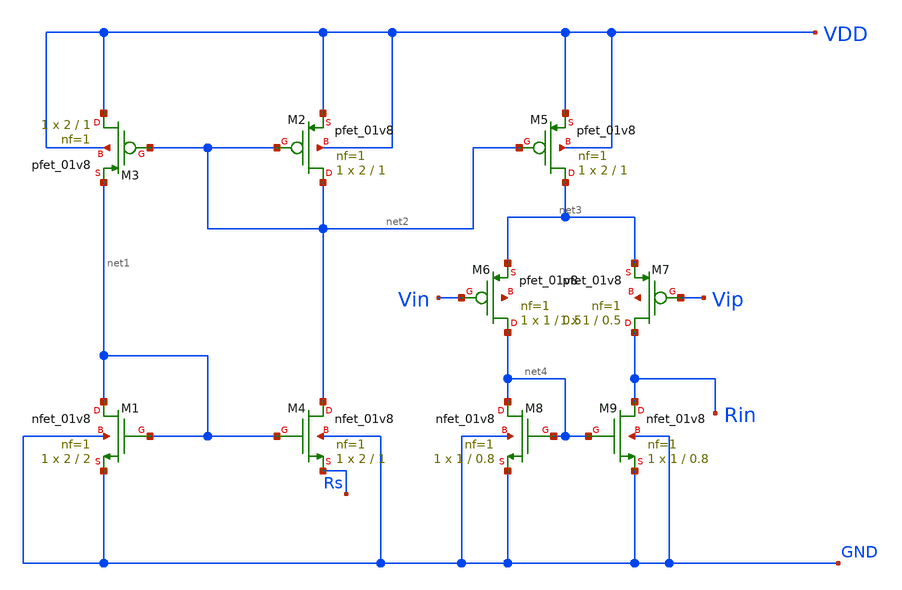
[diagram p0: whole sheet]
** sch_path: opamp.sch
**.subckt opamp
XM1 net1 net1 GND GND sky130_fd_pr__nfet_01v8 L=2 W=2 nf=1 ad='int((nf+1)/2) * W/nf * 0.29' as='int((nf+2)/2) * W/nf * 0.29'
+ pd='2*int((nf+1)/2) * (W/nf + 0.29)' ps='2*int((nf+2)/2) * (W/nf + 0.29)' nrd='0.29 / W' nrs='0.29 / W'
+ sa=0 sb=0 sd=0 mult=1 m=1
XM2 net2 net2 VDD VDD sky130_fd_pr__pfet_01v8 L=1 W=2 nf=1 ad='int((nf+1)/2) * W/nf * 0.29' as='int((nf+2)/2) * W/nf * 0.29'
+ pd='2*int((nf+1)/2) * (W/nf + 0.29)' ps='2*int((nf+2)/2) * (W/nf + 0.29)' nrd='0.29 / W' nrs='0.29 / W'
+ sa=0 sb=0 sd=0 mult=1 m=1
XM3 VDD net2 net1 VDD sky130_fd_pr__pfet_01v8 L=1 W=2 nf=1 ad='int((nf+1)/2) * W/nf * 0.29' as='int((nf+2)/2) * W/nf * 0.29'
+ pd='2*int((nf+1)/2) * (W/nf + 0.29)' ps='2*int((nf+2)/2) * (W/nf + 0.29)' nrd='0.29 / W' nrs='0.29 / W'
+ sa=0 sb=0 sd=0 mult=1 m=1
XM4 net2 net1 Rs GND sky130_fd_pr__nfet_01v8 L=1 W=2 nf=1 ad='int((nf+1)/2) * W/nf * 0.29' as='int((nf+2)/2) * W/nf * 0.29'
+ pd='2*int((nf+1)/2) * (W/nf + 0.29)' ps='2*int((nf+2)/2) * (W/nf + 0.29)' nrd='0.29 / W' nrs='0.29 / W'
+ sa=0 sb=0 sd=0 mult=1 m=1
XM5 net3 net2 VDD VDD sky130_fd_pr__pfet_01v8 L=1 W=2 nf=1 ad='int((nf+1)/2) * W/nf * 0.29' as='int((nf+2)/2) * W/nf * 0.29'
+ pd='2*int((nf+1)/2) * (W/nf + 0.29)' ps='2*int((nf+2)/2) * (W/nf + 0.29)' nrd='0.29 / W' nrs='0.29 / W'
+ sa=0 sb=0 sd=0 mult=1 m=1
XM6 net4 Vin net3 net5 sky130_fd_pr__pfet_01v8 L=0.5 W=1 nf=1 ad='int((nf+1)/2) * W/nf * 0.29' as='int((nf+2)/2) * W/nf * 0.29'
+ pd='2*int((nf+1)/2) * (W/nf + 0.29)' ps='2*int((nf+2)/2) * (W/nf + 0.29)' nrd='0.29 / W' nrs='0.29 / W'
+ sa=0 sb=0 sd=0 mult=1 m=1
XM7 Rin Vip net3 net6 sky130_fd_pr__pfet_01v8 L=0.5 W=1 nf=1 ad='int((nf+1)/2) * W/nf * 0.29' as='int((nf+2)/2) * W/nf * 0.29'
+ pd='2*int((nf+1)/2) * (W/nf + 0.29)' ps='2*int((nf+2)/2) * (W/nf + 0.29)' nrd='0.29 / W' nrs='0.29 / W'
+ sa=0 sb=0 sd=0 mult=1 m=1
XM8 net4 net4 GND GND sky130_fd_pr__nfet_01v8 L=0.8 W=1 nf=1 ad='int((nf+1)/2) * W/nf * 0.29' as='int((nf+2)/2) * W/nf * 0.29'
+ pd='2*int((nf+1)/2) * (W/nf + 0.29)' ps='2*int((nf+2)/2) * (W/nf + 0.29)' nrd='0.29 / W' nrs='0.29 / W'
+ sa=0 sb=0 sd=0 mult=1 m=1
XM9 Rin net4 GND GND sky130_fd_pr__nfet_01v8 L=0.8 W=1 nf=1 ad='int((nf+1)/2) * W/nf * 0.29' as='int((nf+2)/2) * W/nf * 0.29'
+ pd='2*int((nf+1)/2) * (W/nf + 0.29)' ps='2*int((nf+2)/2) * (W/nf + 0.29)' nrd='0.29 / W' nrs='0.29 / W'
+ sa=0 sb=0 sd=0 mult=1 m=1
**.ends
.end
